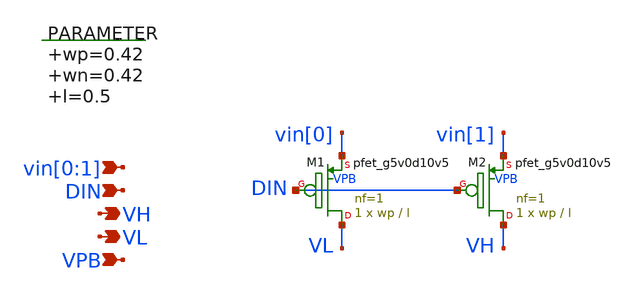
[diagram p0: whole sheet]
** sch_path: xschem/switch_pmos_1g_2o.sch
**.subckt switch_pmos_1g_2o vin[0],vin[1] VH VPB DIN VL
*.ipin vin[0],vin[1]
*.opin VH
*.ipin VPB
*.ipin DIN
*.opin VL
.param wp=0.42 wn=0.42 l=0.5

XM1 VL DIN vin[0] VPB sky130_fd_pr__pfet_g5v0d10v5 L=l W=wp nf=1 ad='int((nf+1)/2) * W/nf * 0.29' as='int((nf+2)/2) * W/nf * 0.29'
+ pd='2*int((nf+1)/2) * (W/nf + 0.29)' ps='2*int((nf+2)/2) * (W/nf + 0.29)' nrd='0.29 / W' nrs='0.29 / W'
+ sa=0 sb=0 sd=0 mult=1 m=1
XM2 VH DIN vin[1] VPB sky130_fd_pr__pfet_g5v0d10v5 L=l W=wp nf=1 ad='int((nf+1)/2) * W/nf * 0.29' as='int((nf+2)/2) * W/nf * 0.29'
+ pd='2*int((nf+1)/2) * (W/nf + 0.29)' ps='2*int((nf+2)/2) * (W/nf + 0.29)' nrd='0.29 / W' nrs='0.29 / W'
+ sa=0 sb=0 sd=0 mult=1 m=1
**.ends
.end
